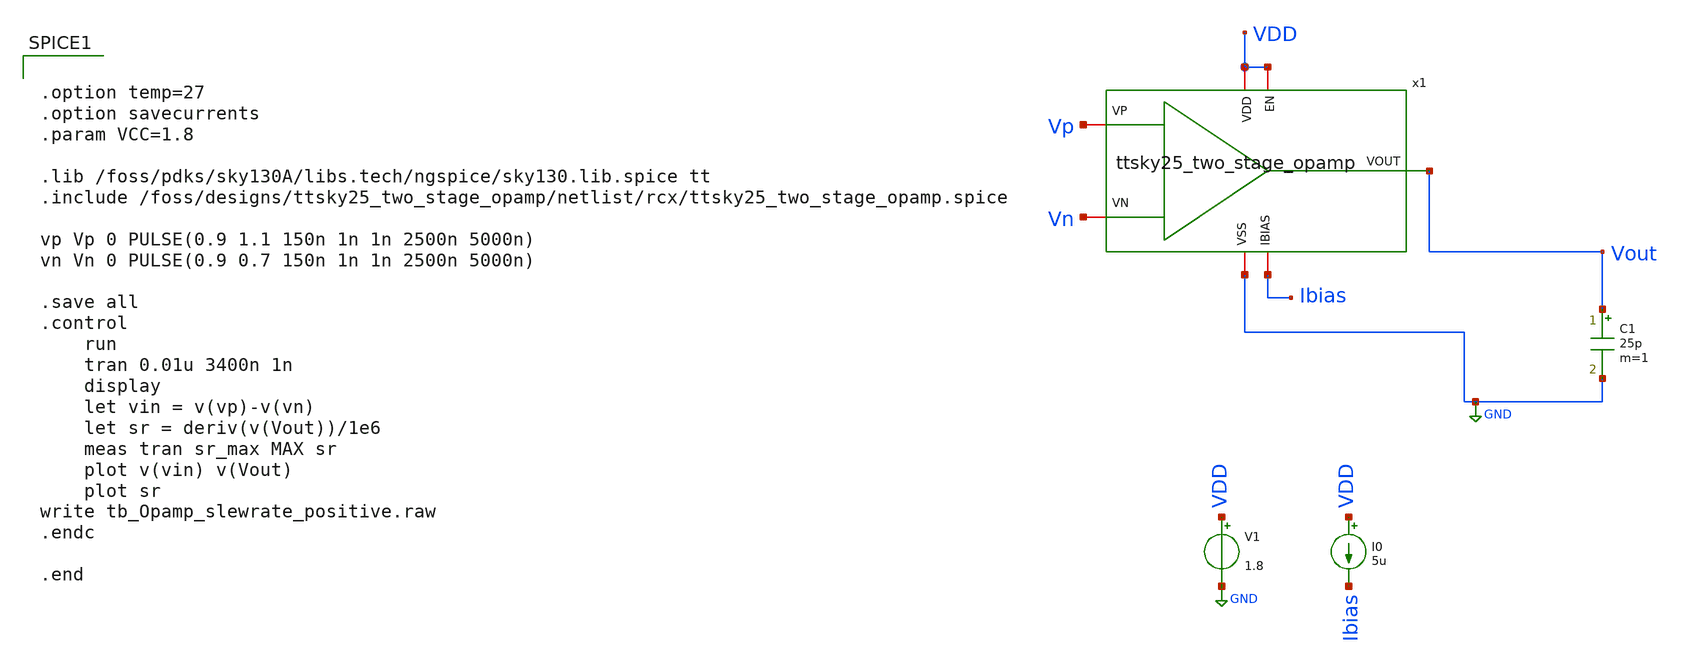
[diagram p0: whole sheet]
** sch_path: xschem/post-layout/testbenches/tb_Opamp_slewrate_positive.sch
**.subckt tb_Opamp_slewrate_positive
V1 VDD GND 1.8
I0 VDD Ibias 5u
C1 Vout GND 25p m=1
x1 VDD Ibias Vout Vn Vp VDD GND ttsky25_two_stage_opamp
**** begin user architecture code


.option temp=27
.option savecurrents
.param VCC=1.8

.lib /foss/pdks/sky130A/libs.tech/ngspice/sky130.lib.spice tt
.include /foss/designs/ttsky25_two_stage_opamp/netlist/rcx/ttsky25_two_stage_opamp.spice

vp Vp 0 PULSE(0.9 1.1 150n 1n 1n 2500n 5000n)
vn Vn 0 PULSE(0.9 0.7 150n 1n 1n 2500n 5000n)

.save all
.control
	run
	tran 0.01u 3400n 1n
	display
	let vin = v(vp)-v(vn)
	let sr = deriv(v(Vout))/1e6
	meas tran sr_max MAX sr
	plot v(vin) v(Vout)
	plot sr
write tb_Opamp_slewrate_positive.raw
.endc

.end


**** end user architecture code
**.ends
.GLOBAL GND
.end
